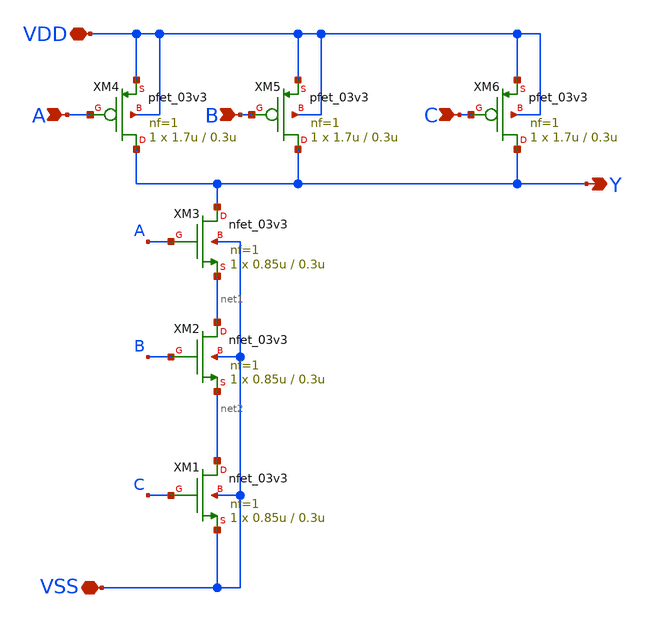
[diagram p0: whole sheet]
** sch_path: gf180mcu_osu_sc_gp12t3v3/xschem/gf180mcu_osu_sc_gp12t3v3__nand3_1.sch
**.subckt gf180mcu_osu_sc_gp12t3v3__nand3_1 A B Y C VDD VSS
*.ipin A
*.ipin B
*.opin Y
*.ipin C
*.iopin VDD
*.iopin VSS
XM1 net2 C VSS VSS nfet_03v3 L=0.3u W=0.85u nf=1 ad='int((nf+1)/2) * W/nf * 0.18u' as='int((nf+2)/2) * W/nf * 0.18u'
+ pd='2*int((nf+1)/2) * (W/nf + 0.18u)' ps='2*int((nf+2)/2) * (W/nf + 0.18u)' nrd='0.18u / W' nrs='0.18u / W'
+ sa=0 sb=0 sd=0 m=1
XM2 net1 B net2 VSS nfet_03v3 L=0.3u W=0.85u nf=1 ad='int((nf+1)/2) * W/nf * 0.18u' as='int((nf+2)/2) * W/nf * 0.18u'
+ pd='2*int((nf+1)/2) * (W/nf + 0.18u)' ps='2*int((nf+2)/2) * (W/nf + 0.18u)' nrd='0.18u / W' nrs='0.18u / W'
+ sa=0 sb=0 sd=0 m=1
XM3 Y A net1 VSS nfet_03v3 L=0.3u W=0.85u nf=1 ad='int((nf+1)/2) * W/nf * 0.18u' as='int((nf+2)/2) * W/nf * 0.18u'
+ pd='2*int((nf+1)/2) * (W/nf + 0.18u)' ps='2*int((nf+2)/2) * (W/nf + 0.18u)' nrd='0.18u / W' nrs='0.18u / W'
+ sa=0 sb=0 sd=0 m=1
XM4 Y A VDD VDD pfet_03v3 L=0.3u W=1.7u nf=1 ad='int((nf+1)/2) * W/nf * 0.18u' as='int((nf+2)/2) * W/nf * 0.18u'
+ pd='2*int((nf+1)/2) * (W/nf + 0.18u)' ps='2*int((nf+2)/2) * (W/nf + 0.18u)' nrd='0.18u / W' nrs='0.18u / W'
+ sa=0 sb=0 sd=0 m=1
XM5 Y B VDD VDD pfet_03v3 L=0.3u W=1.7u nf=1 ad='int((nf+1)/2) * W/nf * 0.18u' as='int((nf+2)/2) * W/nf * 0.18u'
+ pd='2*int((nf+1)/2) * (W/nf + 0.18u)' ps='2*int((nf+2)/2) * (W/nf + 0.18u)' nrd='0.18u / W' nrs='0.18u / W'
+ sa=0 sb=0 sd=0 m=1
XM6 Y C VDD VDD pfet_03v3 L=0.3u W=1.7u nf=1 ad='int((nf+1)/2) * W/nf * 0.18u' as='int((nf+2)/2) * W/nf * 0.18u'
+ pd='2*int((nf+1)/2) * (W/nf + 0.18u)' ps='2*int((nf+2)/2) * (W/nf + 0.18u)' nrd='0.18u / W' nrs='0.18u / W'
+ sa=0 sb=0 sd=0 m=1
**.ends
.end
